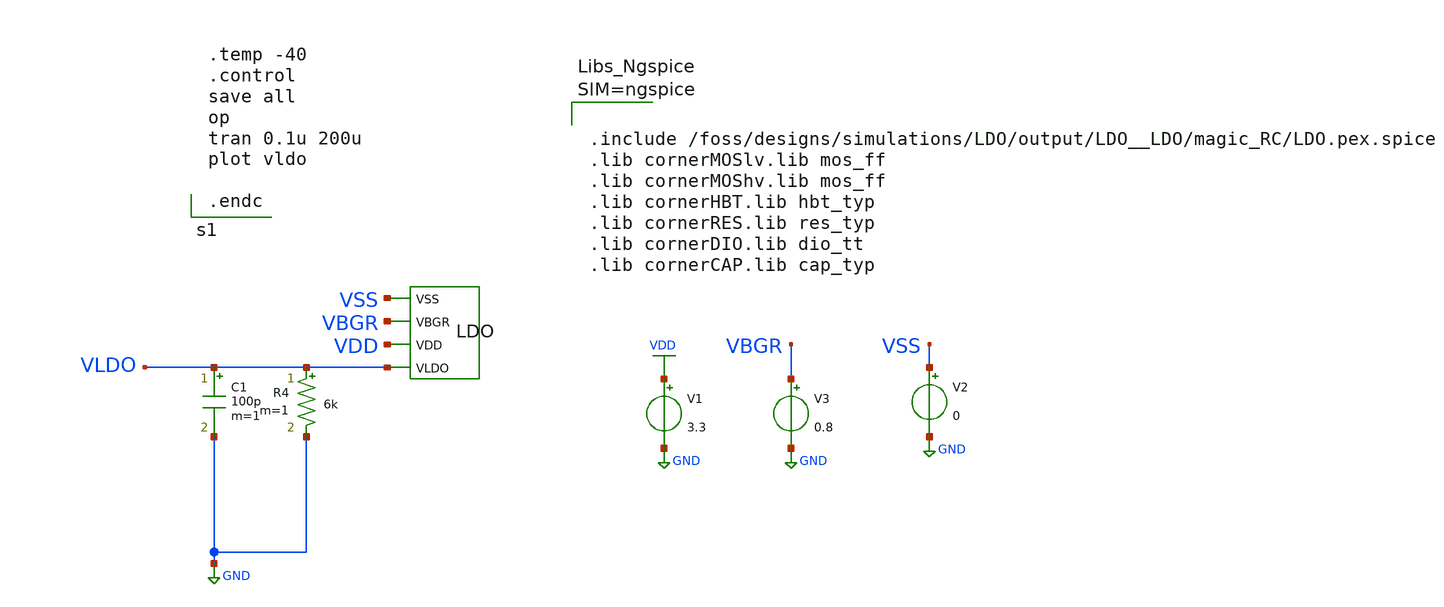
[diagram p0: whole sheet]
** sch_path: dependencies/LDO/LDO-main/testbenches/corners/xschem/ldo_post_layout_sim_ff_m40C.sch
**.subckt ldo_post_layout_sim_ff_m40C
V1 VDD GND 3.3
V3 VBGR GND 0.8
V2 VSS GND 0
X1 VSS VBGR VDD VLDO LDO
C1 VLDO GND 100p m=1
R4 VLDO GND 6k m=1
**** begin user architecture code



.include /foss/designs/simulations/LDO/output/LDO__LDO/magic_RC/LDO.pex.spice
.lib cornerMOSlv.lib mos_ff
.lib cornerMOShv.lib mos_ff
.lib cornerHBT.lib hbt_typ
.lib cornerRES.lib res_typ
.lib cornerDIO.lib dio_tt
.lib cornerCAP.lib cap_typ





.temp -40
.control
save all
op
tran 0.1u 200u
plot vldo

.endc

**** end user architecture code
**.ends
.GLOBAL GND
.GLOBAL VDD
.end
